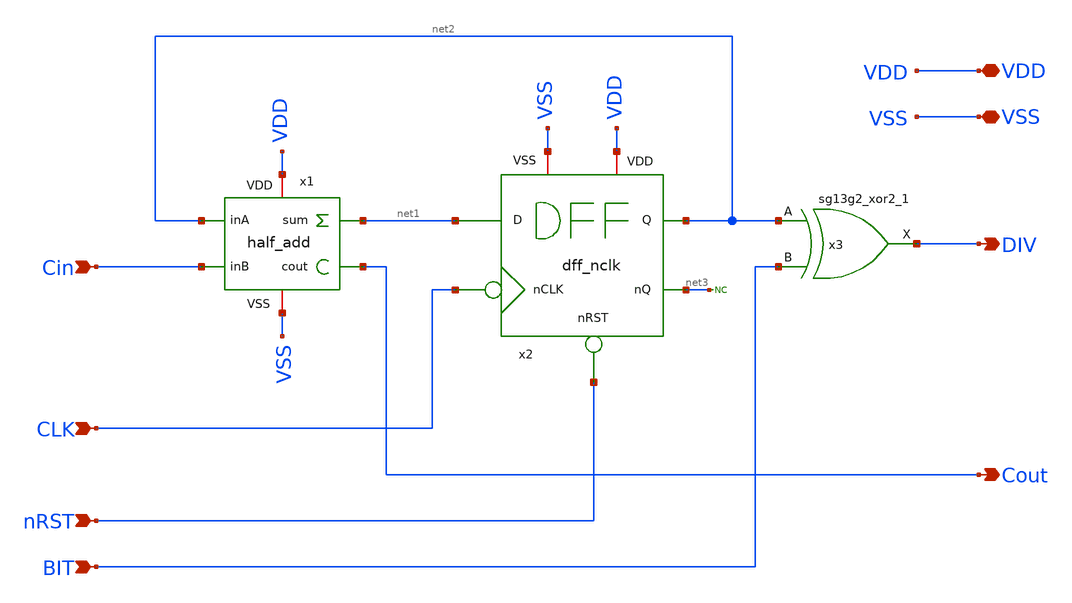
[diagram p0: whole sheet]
** sch_path: Combined Design/design_data/xschem/freq_div_cell.sch
**.subckt freq_div_cell Cin CLK nRST BIT DIV Cout VSS VDD
*.ipin Cin
*.ipin CLK
*.ipin nRST
*.ipin BIT
*.opin DIV
*.opin Cout
*.iopin VSS
*.iopin VDD
x1 net2 net1 Cin VDD VSS Cout half_add
x2 CLK net2 net1 net3 nRST VDD VSS dff_nclk
x3 DIV net2 BIT VDD VSS sg13g2_xor2_1
* noconn #net3
**.ends
.end
